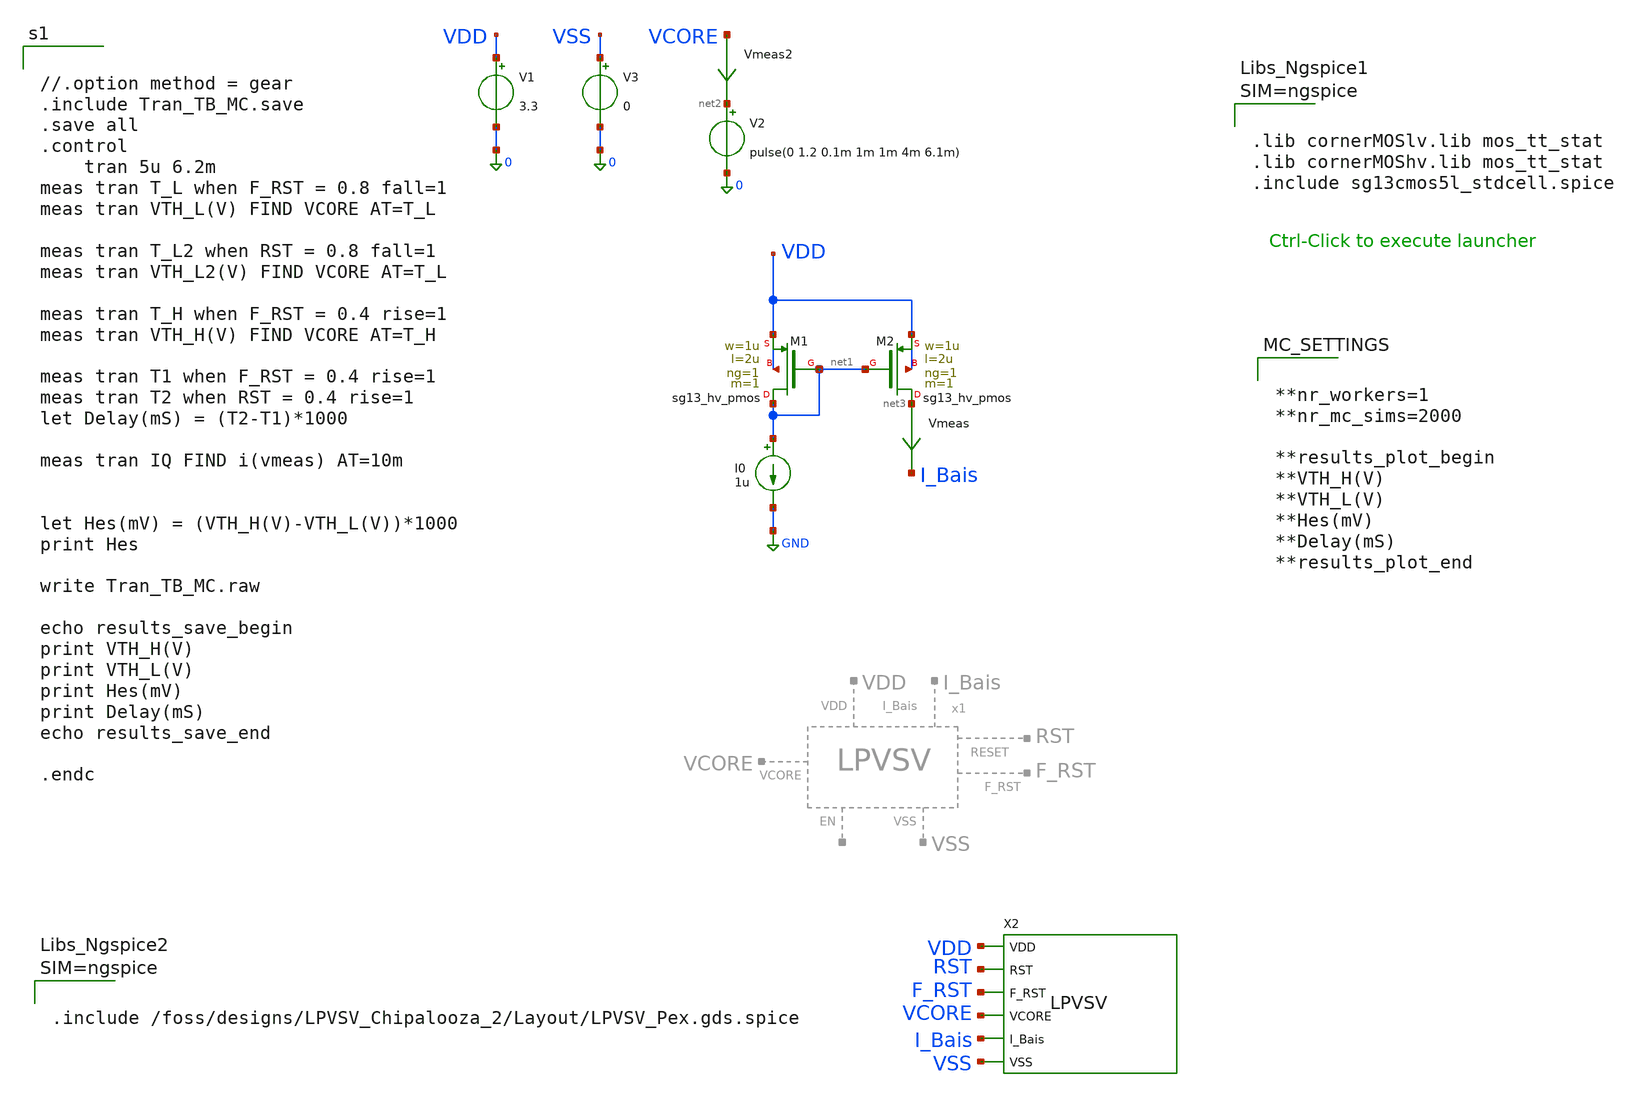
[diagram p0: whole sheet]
** sch_path: Simulation/Tran_TB_MC.sch
**.subckt Tran_TB_MC
V1 VDD 0 3.3
V2 net2 0 pulse(0 1.2 0.1m 1m 1m 4m 6.1m)
Vmeas2 VCORE net2 0
.save i(vmeas2)
V3 VSS 0 0
X2 VSS F_RST VDD VCORE I_Bais RST LPVSV
I0 net1 GND 1u
Vmeas net3 I_Bais 0
.save i(vmeas)
XM1 net1 net1 VDD VDD sg13_hv_pmos w=1u l=2u ng=1 m=1 mm_ok=1
XM2 net3 net1 VDD VDD sg13_hv_pmos w=1u l=2u ng=1 m=1 mm_ok=1
**** begin user architecture code



.lib cornerMOSlv.lib mos_tt_stat
.lib cornerMOShv.lib mos_tt_stat
.include sg13cmos5l_stdcell.spice





**nr_workers=1
**nr_mc_sims=2000

**results_plot_begin
**VTH_H(V)
**VTH_L(V)
**Hes(mV)
**Delay(mS)
**results_plot_end




//.option method = gear
.include Tran_TB_MC.save
.save all
.control
	tran 5u 6.2m
meas tran T_L when F_RST = 0.8 fall=1
meas tran VTH_L(V) FIND VCORE AT=T_L

meas tran T_L2 when RST = 0.8 fall=1
meas tran VTH_L2(V) FIND VCORE AT=T_L

meas tran T_H when F_RST = 0.4 rise=1
meas tran VTH_H(V) FIND VCORE AT=T_H

meas tran T1 when F_RST = 0.4 rise=1
meas tran T2 when RST = 0.4 rise=1
let Delay(mS) = (T2-T1)*1000

meas tran IQ FIND i(vmeas) AT=10m


let Hes(mV) = (VTH_H(V)-VTH_L(V))*1000
print Hes

write Tran_TB_MC.raw

echo results_save_begin
print VTH_H(V)
print VTH_L(V)
print Hes(mV)
print Delay(mS)
echo results_save_end

.endc





.include /foss/designs/LPVSV_Chipalooza_2/Layout/LPVSV_Pex.gds.spice



**** end user architecture code
**.ends
.GLOBAL GND
.end
